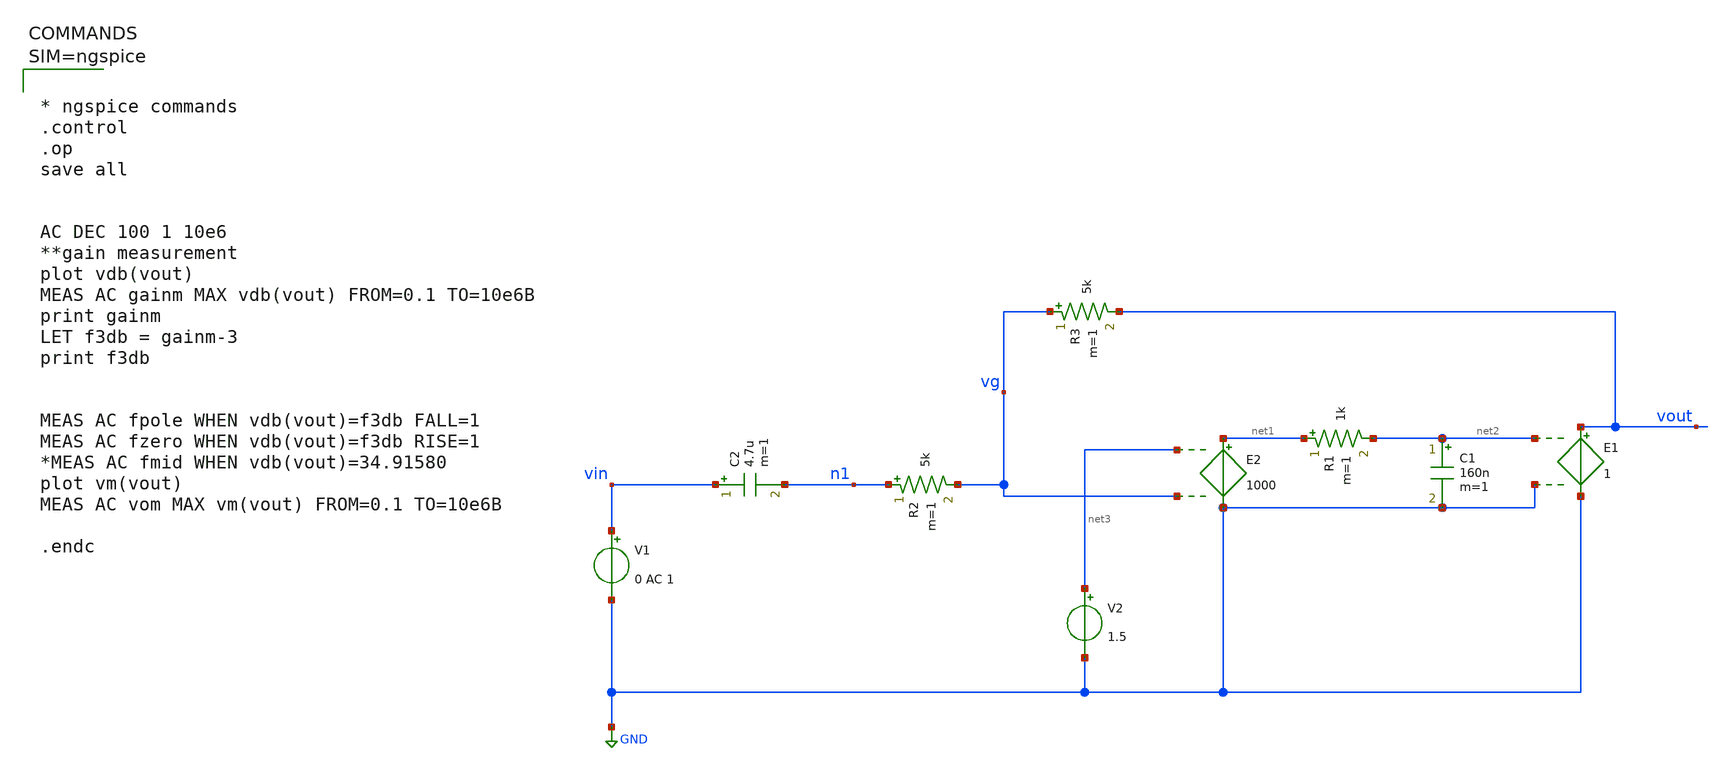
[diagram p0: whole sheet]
** sch_path: highPass_Cascade.sch
**.subckt highPass_Cascade
E1 vout GND net2 GND 1
E2 net1 GND net3 vg 1000
C1 net2 GND 160n m=1
R1 net1 net2 1k m=1
V1 vin GND 0 AC 1
C2 vin n1 4.7u m=1
R2 n1 vg 5k m=1
R3 vg vout 5k m=1
V2 net3 GND 1.5
**** begin user architecture code



* ngspice commands
.control
.op
save all


AC DEC 100 1 10e6
**gain measurement
plot vdb(vout)
MEAS AC gainm MAX vdb(vout) FROM=0.1 TO=10e6B
print gainm
LET f3db = gainm-3
print f3db


MEAS AC fpole WHEN vdb(vout)=f3db FALL=1
MEAS AC fzero WHEN vdb(vout)=f3db RISE=1
*MEAS AC fmid WHEN vdb(vout)=34.91580
plot vm(vout)
MEAS AC vom MAX vm(vout) FROM=0.1 TO=10e6B

.endc



**** end user architecture code
**.ends
.GLOBAL GND
.end
